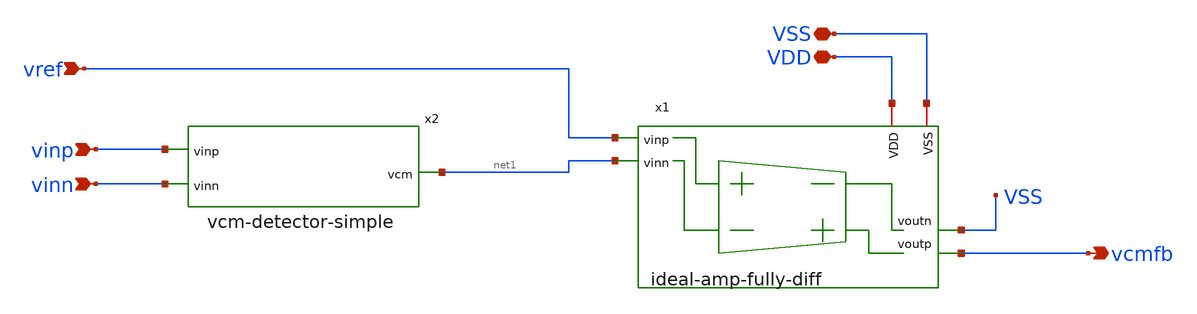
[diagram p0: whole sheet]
** sch_path: analog-db/circuits/cmfb_001_ideal_rsense_servo/pdk/ihp-sg13g2/schematic/cmfb-output-ideal-amp.sch
* Copyright 2026 MacAnalog Research Group
**.subckt cmfb-output-ideal-amp VSS VDD vinp vinn vcmfb vref
*.iopin VSS
*.iopin VDD
*.ipin vinp
*.ipin vinn
*.opin vcmfb
*.ipin vref
x1 vref net1 VSS vcmfb VSS VDD ideal-amp-fully-diff
x2 net1 vinp vinn vcm-detector-simple
**.ends
.end
